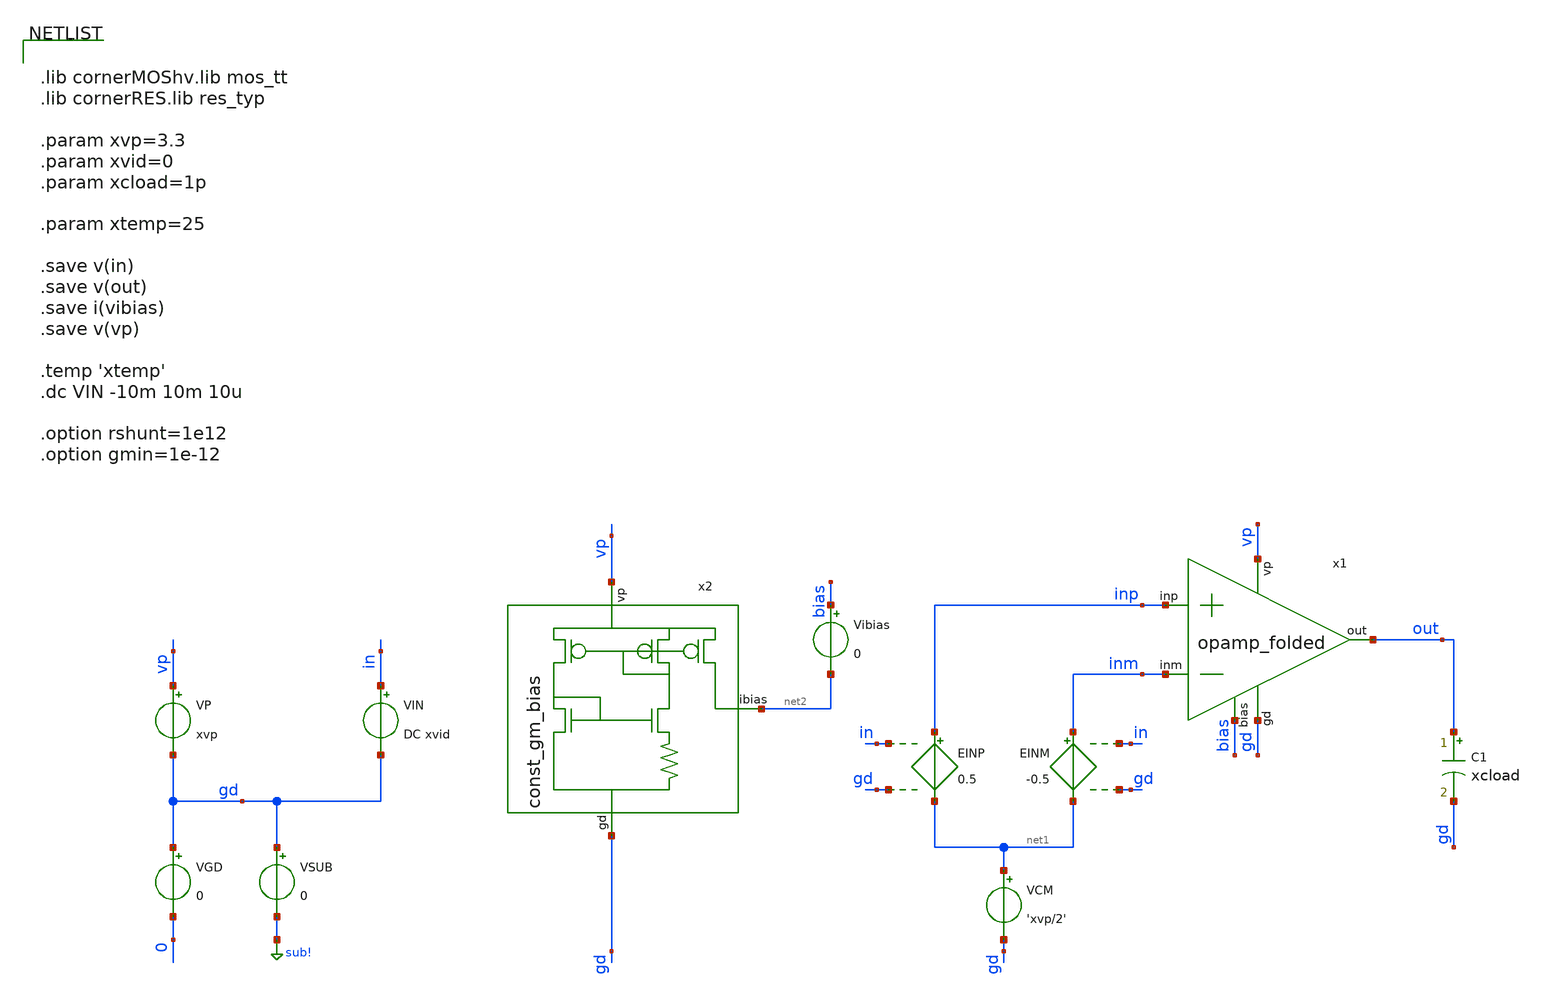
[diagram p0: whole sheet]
** sch_path: testbench/opamp_dc_tb.sch
**.subckt opamp_dc_tb
EINP inp net1 in gd 0.5
EINM inm net1 in gd -0.5
C1 out gd xcload m=1
VGD gd 0 0
VP vp gd xvp
VSUB gd sub! 0
VIN in gd DC xvid
VCM net1 gd 'xvp/2'
Vibias bias net2 0
.save i(vibias)
x1 vp inp inm out bias gd opamp_folded
x2 vp net2 gd const_gm_bias
**** begin user architecture code


.lib cornerMOShv.lib mos_tt
.lib cornerRES.lib res_typ

.param xvp=3.3
.param xvid=0
.param xcload=1p

.param xtemp=25

.save v(in)
.save v(out)
.save i(vibias)
.save v(vp)

.temp 'xtemp'
.dc VIN -10m 10m 10u

.option rshunt=1e12
.option gmin=1e-12


**** end user architecture code
**.ends
.GLOBAL sub!
.end
